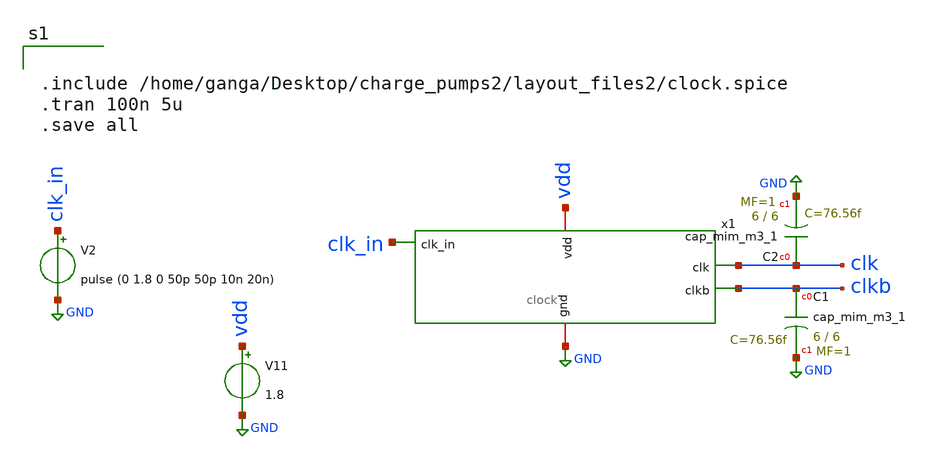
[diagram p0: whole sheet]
** sch_path: xschem/charge_pumps2/clock_port_layout.sch
**.subckt clock_port_layout
V2 clk_in GND pulse (0 1.8 0 50p 50p 10n 20n)
V11 vdd GND 1.8
x1 clk_in vdd GND clk clkb clock
XC1 clkb GND sky130_fd_pr__cap_mim_m3_1 W=6 L=6 MF=1 m=1
XC2 clk GND sky130_fd_pr__cap_mim_m3_1 W=6 L=6 MF=1 m=1
**** begin user architecture code

** opencircuitdesign pdks install
.lib $::SKYWATER_MODELS/sky130.lib.spice tt




.include /home/ganga/Desktop/charge_pumps2/layout_files2/clock.spice
.tran 100n 5u
.save all


**** end user architecture code
**.ends
.GLOBAL GND
.end
